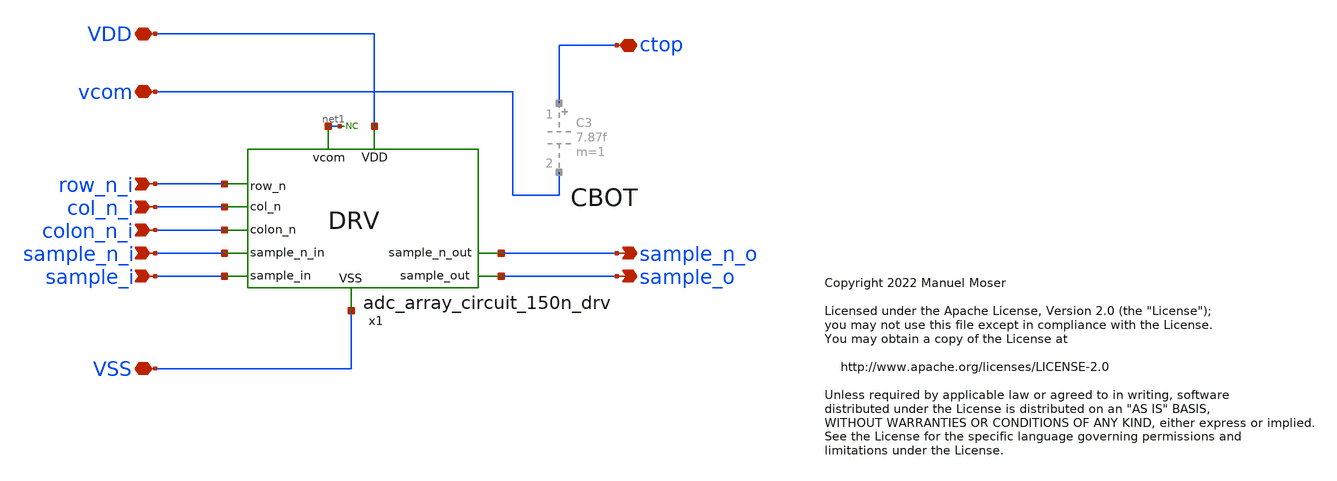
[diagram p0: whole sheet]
** sch_path: xschem/adc_array_cap_150n/adc_array_cap_drv.sch
* Copyright 2022 Manuel Moser
* Licensed under the Apache License, Version 2.0 (the "License");
**.subckt adc_array_cap_drv sample_n_i sample_i vcom VDD ctop VSS sample_n_o sample_o row_n_i
*+ col_n_i colon_n_i
*.ipin sample_n_i
*.ipin sample_i
*.iopin vcom
*.iopin VDD
*.iopin ctop
*.iopin VSS
*.opin sample_n_o
*.opin sample_o
*.ipin row_n_i
*.ipin col_n_i
*.ipin colon_n_i
x1 VDD row_n_i col_n_i colon_n_i sample_n_i net1 sample_i VSS sample_n_o sample_o
+ adc_array_circuit_150n_drv
* noconn #net1
**.ends

* expanding   symbol:
*+  /foss/designs/SKY130_SAR-ADC/xschem/adc_array_circuit_150n/adc_array_circuit_150n_drv.sym # of pins=10
** sym_path: xschem/adc_array_circuit_150n/adc_array_circuit_150n_drv.sym
** sch_path: xschem/adc_array_circuit_150n/adc_array_circuit_150n_drv.sch
.subckt adc_array_circuit_150n_drv VDD row_n col_n colon_n sample_n_in vcom sample_in VSS
+ sample_n_out sample_out
*.ipin sample_n_in
*.ipin sample_in
*.iopin vcom
*.ipin row_n
*.ipin col_n
*.ipin colon_n
*.iopin VDD
*.iopin VSS
*.opin sample_out
*.opin sample_n_out
XM6 VDD sample_n_in sample_out VDD sky130_fd_pr__pfet_01v8 L=0.15 W=1.6 nf=1 ad='int((nf+1)/2) * W/nf * 0.29'
+ as='int((nf+2)/2) * W/nf * 0.29' pd='2*int((nf+1)/2) * (W/nf + 0.29)' ps='2*int((nf+2)/2) * (W/nf + 0.29)'
+ nrd='0.29 / W' nrs='0.29 / W' sa=0 sb=0 sd=0 mult=1 m=1
XM7 VDD sample_in sample_n_out VDD sky130_fd_pr__pfet_01v8 L=0.15 W=1.6 nf=1 ad='int((nf+1)/2) * W/nf * 0.29'
+ as='int((nf+2)/2) * W/nf * 0.29' pd='2*int((nf+1)/2) * (W/nf + 0.29)' ps='2*int((nf+2)/2) * (W/nf + 0.29)'
+ nrd='0.29 / W' nrs='0.29 / W' sa=0 sb=0 sd=0 mult=1 m=1
XM9 VSS sample_in sample_n_out VSS sky130_fd_pr__nfet_01v8 L=0.15 W=0.84 nf=1 ad='int((nf+1)/2) * W/nf * 0.29'
+ as='int((nf+2)/2) * W/nf * 0.29' pd='2*int((nf+1)/2) * (W/nf + 0.29)' ps='2*int((nf+2)/2) * (W/nf + 0.29)'
+ nrd='0.29 / W' nrs='0.29 / W' sa=0 sb=0 sd=0 mult=1 m=1
XM10 VSS sample_n_in sample_out VSS sky130_fd_pr__nfet_01v8 L=0.15 W=0.84 nf=1 ad='int((nf+1)/2) * W/nf * 0.29'
+ as='int((nf+2)/2) * W/nf * 0.29' pd='2*int((nf+1)/2) * (W/nf + 0.29)' ps='2*int((nf+2)/2) * (W/nf + 0.29)'
+ nrd='0.29 / W' nrs='0.29 / W' sa=0 sb=0 sd=0 mult=1 m=1
* noconn row_n
* noconn col_n
* noconn colon_n
* noconn vcom
.ends

.end
